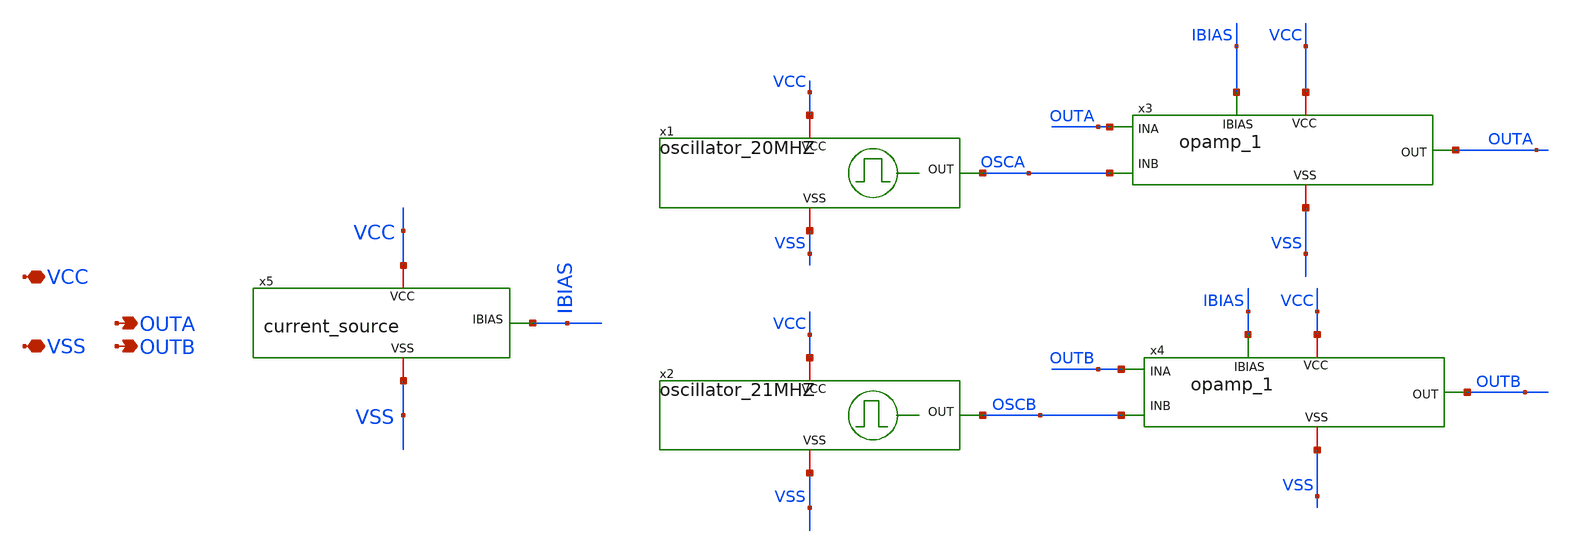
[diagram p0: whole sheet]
** sch_path: xschem/top.sch
**.subckt top VCC VSS OUTA OUTB
*.iopin VCC
*.iopin VSS
*.opin OUTA
*.opin OUTB
x1 VCC OSCA VSS oscillator_20MHZ
x2 VCC OSCB VSS oscillator_21MHZ
x3 VCC OUTA OUTA OSCA VSS IBIAS opamp_1
x4 VCC OUTB OUTB OSCB VSS IBIAS opamp_1
x5 VCC VSS IBIAS current_source
**.ends

* expanding   symbol:  oscillator_20MHZ.sym # of pins=3
** sym_path: xschem/oscillator_20MHZ.sym
** sch_path: xschem/oscillator_20MHZ.sch
.subckt oscillator_20MHZ VCC OUT VSS
*.iopin VCC
*.iopin VSS
*.opin OUT
x1[30] INI[29] OUT_INI VCC VSS inverter
x1[29] INI[28] INI[29] VCC VSS inverter
x1[28] INI[27] INI[28] VCC VSS inverter
x1[27] INI[26] INI[27] VCC VSS inverter
x1[26] INI[25] INI[26] VCC VSS inverter
x1[25] INI[24] INI[25] VCC VSS inverter
x1[24] INI[23] INI[24] VCC VSS inverter
x1[23] INI[22] INI[23] VCC VSS inverter
x1[22] INI[21] INI[22] VCC VSS inverter
x1[21] INI[20] INI[21] VCC VSS inverter
x1[20] INI[19] INI[20] VCC VSS inverter
x1[19] INI[18] INI[19] VCC VSS inverter
x1[18] INI[17] INI[18] VCC VSS inverter
x1[17] INI[16] INI[17] VCC VSS inverter
x1[16] INI[15] INI[16] VCC VSS inverter
x1[15] INI[14] INI[15] VCC VSS inverter
x1[14] INI[13] INI[14] VCC VSS inverter
x1[13] INI[12] INI[13] VCC VSS inverter
x1[12] INI[11] INI[12] VCC VSS inverter
x1[11] INI[10] INI[11] VCC VSS inverter
x1[10] INI[9] INI[10] VCC VSS inverter
x1[9] INI[8] INI[9] VCC VSS inverter
x1[8] INI[7] INI[8] VCC VSS inverter
x1[7] INI[6] INI[7] VCC VSS inverter
x1[6] INI[5] INI[6] VCC VSS inverter
x1[5] INI[4] INI[5] VCC VSS inverter
x1[4] INI[3] INI[4] VCC VSS inverter
x1[3] INI[2] INI[3] VCC VSS inverter
x1[2] INI[1] INI[2] VCC VSS inverter
x1[1] INI[0] INI[1] VCC VSS inverter
x1[0] OUT_INI INI[0] VCC VSS inverter
x3 OUT OUT_INI VCC VSS inverter
.ends


* expanding   symbol:  oscillator_21MHZ.sym # of pins=3
** sym_path: xschem/oscillator_21MHZ.sym
** sch_path: xschem/oscillator_21MHZ.sch
.subckt oscillator_21MHZ VCC OUT VSS
*.iopin VCC
*.iopin VSS
*.opin OUT
x1[20] INI[19] OUT_INI VCC VSS inverter
x1[19] INI[18] INI[19] VCC VSS inverter
x1[18] INI[17] INI[18] VCC VSS inverter
x1[17] INI[16] INI[17] VCC VSS inverter
x1[16] INI[15] INI[16] VCC VSS inverter
x1[15] INI[14] INI[15] VCC VSS inverter
x1[14] INI[13] INI[14] VCC VSS inverter
x1[13] INI[12] INI[13] VCC VSS inverter
x1[12] INI[11] INI[12] VCC VSS inverter
x1[11] INI[10] INI[11] VCC VSS inverter
x1[10] INI[9] INI[10] VCC VSS inverter
x1[9] INI[8] INI[9] VCC VSS inverter
x1[8] INI[7] INI[8] VCC VSS inverter
x1[7] INI[6] INI[7] VCC VSS inverter
x1[6] INI[5] INI[6] VCC VSS inverter
x1[5] INI[4] INI[5] VCC VSS inverter
x1[4] INI[3] INI[4] VCC VSS inverter
x1[3] INI[2] INI[3] VCC VSS inverter
x1[2] INI[1] INI[2] VCC VSS inverter
x1[1] INI[0] INI[1] VCC VSS inverter
x1[0] OUT_INI INI[0] VCC VSS inverter
x1 OUT OUT_INI VCC VSS inverter
.ends


* expanding   symbol:  opamp_1.sym # of pins=6
** sym_path: xschem/opamp_1.sym
** sch_path: xschem/opamp_1.sch
.subckt opamp_1 VCC OUT INA INB VSS IBIAS
*.ipin INA
*.ipin INB
*.opin OUT
*.iopin VCC
*.iopin VSS
*.ipin IBIAS
x1 DIFF_OUT MIRR INA INB TAILV VSS indiff
x2 VCC DIFF_OUT MIRR activeload
x3 VCC IBIAS DIFF_OUT RN VSS active-resistor
x4 TAILV IBIAS VSS tail_current
x5 VCC DIFF_OUT OUT IBIAS VSS second_stage
XC2 RN OUT sky130_fd_pr__cap_mim_m3_1 W=20 L=13 MF=1 m=1
.ends


* expanding   symbol:  current_source.sym # of pins=3
** sym_path: xschem/current_source.sym
** sch_path: xschem/current_source.sch
.subckt current_source VCC VSS IBIAS
*.iopin VCC
*.iopin VSS
*.opin IBIAS
XM3 IBIAS IBIAS VSS VSS sky130_fd_pr__nfet_01v8 L=1 W=40 nf=1 ad='int((nf+1)/2) * W/nf * 0.29' as='int((nf+2)/2) * W/nf * 0.29'
+ pd='2*int((nf+1)/2) * (W/nf + 0.29)' ps='2*int((nf+2)/2) * (W/nf + 0.29)' nrd='0.29 / W' nrs='0.29 / W'
+ sa=0 sb=0 sd=0 mult=1 m=1
XR1 IBIAS VCC VSS sky130_fd_pr__res_xhigh_po W=1 L=9 mult=1 m=1
.ends


* expanding   symbol:  inverter.sym # of pins=4
** sym_path: xschem/inverter.sym
** sch_path: xschem/inverter.sch
.subckt inverter OUT IN VCC VSS
*.iopin VCC
*.iopin VSS
*.ipin IN
*.opin OUT
XM1 OUT IN net1 VCC sky130_fd_pr__pfet_01v8 L=1 W=2 nf=1 ad='int((nf+1)/2) * W/nf * 0.29' as='int((nf+2)/2) * W/nf * 0.29'
+ pd='2*int((nf+1)/2) * (W/nf + 0.29)' ps='2*int((nf+2)/2) * (W/nf + 0.29)' nrd='0.29 / W' nrs='0.29 / W'
+ sa=0 sb=0 sd=0 mult=1 m=1
XM2 OUT IN net2 VSS sky130_fd_pr__nfet_01v8 L=1 W=1 nf=1 ad='int((nf+1)/2) * W/nf * 0.29' as='int((nf+2)/2) * W/nf * 0.29'
+ pd='2*int((nf+1)/2) * (W/nf + 0.29)' ps='2*int((nf+2)/2) * (W/nf + 0.29)' nrd='0.29 / W' nrs='0.29 / W'
+ sa=0 sb=0 sd=0 mult=1 m=1
XM3 net1 VSS VCC VCC sky130_fd_pr__pfet_01v8 L=1 W=2 nf=1 ad='int((nf+1)/2) * W/nf * 0.29' as='int((nf+2)/2) * W/nf * 0.29'
+ pd='2*int((nf+1)/2) * (W/nf + 0.29)' ps='2*int((nf+2)/2) * (W/nf + 0.29)' nrd='0.29 / W' nrs='0.29 / W'
+ sa=0 sb=0 sd=0 mult=1 m=1
XM4 net2 VCC VSS VSS sky130_fd_pr__nfet_01v8 L=1 W=1 nf=1 ad='int((nf+1)/2) * W/nf * 0.29' as='int((nf+2)/2) * W/nf * 0.29'
+ pd='2*int((nf+1)/2) * (W/nf + 0.29)' ps='2*int((nf+2)/2) * (W/nf + 0.29)' nrd='0.29 / W' nrs='0.29 / W'
+ sa=0 sb=0 sd=0 mult=1 m=1
.ends


* expanding   symbol:  indiff.sym # of pins=6
** sym_path: xschem/indiff.sym
** sch_path: xschem/indiff.sch
.subckt indiff DB DA INA INB S VSS
*.ipin INA
*.ipin INB
*.iopin DA
*.iopin DB
*.iopin S
*.iopin VSS
XM1 DA INA S VSS sky130_fd_pr__nfet_01v8 L=1 W=5 nf=1 ad='int((nf+1)/2) * W/nf * 0.29' as='int((nf+2)/2) * W/nf * 0.29'
+ pd='2*int((nf+1)/2) * (W/nf + 0.29)' ps='2*int((nf+2)/2) * (W/nf + 0.29)' nrd='0.29 / W' nrs='0.29 / W'
+ sa=0 sb=0 sd=0 mult=4 m=4
XM2 DB INB S VSS sky130_fd_pr__nfet_01v8 L=1 W=5 nf=1 ad='int((nf+1)/2) * W/nf * 0.29' as='int((nf+2)/2) * W/nf * 0.29'
+ pd='2*int((nf+1)/2) * (W/nf + 0.29)' ps='2*int((nf+2)/2) * (W/nf + 0.29)' nrd='0.29 / W' nrs='0.29 / W'
+ sa=0 sb=0 sd=0 mult=4 m=4
.ends


* expanding   symbol:  activeload.sym # of pins=3
** sym_path: xschem/activeload.sym
** sch_path: xschem/activeload.sch
.subckt activeload VCC DB DA
*.iopin DA
*.iopin DB
*.iopin VCC
XM4 DA DA VCC VCC sky130_fd_pr__pfet_01v8_lvt L=0.5 W=5 nf=1 ad='int((nf+1)/2) * W/nf * 0.29' as='int((nf+2)/2) * W/nf * 0.29'
+ pd='2*int((nf+1)/2) * (W/nf + 0.29)' ps='2*int((nf+2)/2) * (W/nf + 0.29)' nrd='0.29 / W' nrs='0.29 / W'
+ sa=0 sb=0 sd=0 mult=3 m=3
XM5 DB DA VCC VCC sky130_fd_pr__pfet_01v8_lvt L=0.5 W=5 nf=1 ad='int((nf+1)/2) * W/nf * 0.29' as='int((nf+2)/2) * W/nf * 0.29'
+ pd='2*int((nf+1)/2) * (W/nf + 0.29)' ps='2*int((nf+2)/2) * (W/nf + 0.29)' nrd='0.29 / W' nrs='0.29 / W'
+ sa=0 sb=0 sd=0 mult=3 m=3
.ends


* expanding   symbol:  active-resistor.sym # of pins=5
** sym_path: xschem/active-resistor.sym
** sch_path: xschem/active-resistor.sch
.subckt active-resistor VCC IBIAS RP RN VSS
*.iopin VCC
*.iopin VSS
*.ipin IBIAS
*.iopin RP
*.iopin RN
XM9 RBIAS IBIAS VSS VSS sky130_fd_pr__nfet_01v8 L=1 W=5 nf=1 ad='int((nf+1)/2) * W/nf * 0.29' as='int((nf+2)/2) * W/nf * 0.29'
+ pd='2*int((nf+1)/2) * (W/nf + 0.29)' ps='2*int((nf+2)/2) * (W/nf + 0.29)' nrd='0.29 / W' nrs='0.29 / W'
+ sa=0 sb=0 sd=0 mult=1 m=1
XM10 RBIAS RBIAS net1 VCC sky130_fd_pr__pfet_01v8_lvt L=0.5 W=1 nf=1 ad='int((nf+1)/2) * W/nf * 0.29'
+ as='int((nf+2)/2) * W/nf * 0.29' pd='2*int((nf+1)/2) * (W/nf + 0.29)' ps='2*int((nf+2)/2) * (W/nf + 0.29)'
+ nrd='0.29 / W' nrs='0.29 / W' sa=0 sb=0 sd=0 mult=1 m=1
XM11 net1 net1 VCC VCC sky130_fd_pr__pfet_01v8_lvt L=0.5 W=7.5 nf=1 ad='int((nf+1)/2) * W/nf * 0.29'
+ as='int((nf+2)/2) * W/nf * 0.29' pd='2*int((nf+1)/2) * (W/nf + 0.29)' ps='2*int((nf+2)/2) * (W/nf + 0.29)'
+ nrd='0.29 / W' nrs='0.29 / W' sa=0 sb=0 sd=0 mult=1 m=1
XM8 RN RBIAS RP VCC sky130_fd_pr__pfet_01v8_lvt L=0.5 W=7 nf=1 ad='int((nf+1)/2) * W/nf * 0.29' as='int((nf+2)/2) * W/nf * 0.29'
+ pd='2*int((nf+1)/2) * (W/nf + 0.29)' ps='2*int((nf+2)/2) * (W/nf + 0.29)' nrd='0.29 / W' nrs='0.29 / W'
+ sa=0 sb=0 sd=0 mult=2 m=2
.ends


* expanding   symbol:  tail_current.sym # of pins=3
** sym_path: xschem/tail_current.sym
** sch_path: xschem/tail_current.sch
.subckt tail_current TAILV IBIAS VSS
*.iopin VSS
*.ipin IBIAS
*.iopin TAILV
XM3 TAILV IBIAS VSS VSS sky130_fd_pr__nfet_01v8 L=1 W=5 nf=1 ad='int((nf+1)/2) * W/nf * 0.29' as='int((nf+2)/2) * W/nf * 0.29'
+ pd='2*int((nf+1)/2) * (W/nf + 0.29)' ps='2*int((nf+2)/2) * (W/nf + 0.29)' nrd='0.29 / W' nrs='0.29 / W'
+ sa=0 sb=0 sd=0 mult=8 m=8
.ends


* expanding   symbol:  second_stage.sym # of pins=5
** sym_path: xschem/second_stage.sym
** sch_path: xschem/second_stage.sch
.subckt second_stage VCC DIFF_OUT OUT IBIAS VSS
*.iopin VCC
*.iopin VSS
*.ipin IBIAS
*.ipin DIFF_OUT
*.opin OUT
XM6 OUT IBIAS VSS VSS sky130_fd_pr__nfet_01v8 L=0.5 W=5 nf=1 ad='int((nf+1)/2) * W/nf * 0.29' as='int((nf+2)/2) * W/nf * 0.29'
+ pd='2*int((nf+1)/2) * (W/nf + 0.29)' ps='2*int((nf+2)/2) * (W/nf + 0.29)' nrd='0.29 / W' nrs='0.29 / W'
+ sa=0 sb=0 sd=0 mult=19 m=19
XM2 OUT DIFF_OUT VCC VCC sky130_fd_pr__pfet_01v8_lvt L=0.5 W=5 nf=1 ad='int((nf+1)/2) * W/nf * 0.29'
+ as='int((nf+2)/2) * W/nf * 0.29' pd='2*int((nf+1)/2) * (W/nf + 0.29)' ps='2*int((nf+2)/2) * (W/nf + 0.29)'
+ nrd='0.29 / W' nrs='0.29 / W' sa=0 sb=0 sd=0 mult=14 m=14
.ends

.end
